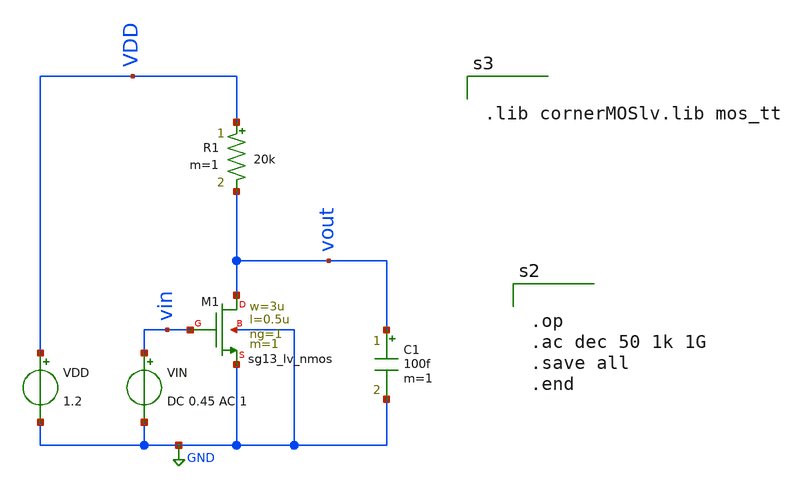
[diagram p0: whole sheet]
** sch_path: BTDay3-Ex/Ex1_Lecture3_1.sch
**.subckt Ex1_Lecture3_1
XM1 vout vin GND GND sg13_lv_nmos w=3u l=0.5u ng=1 m=1 mm_ok=1
VDD VDD GND 1.2
VIN vin GND DC 0.45 AC 1
R1 VDD vout 20k m=1
C1 vout GND 100f m=1
**** begin user architecture code


.op
.ac dec 50 1k 1G
.save all
.end




.lib cornerMOSlv.lib mos_tt


**** end user architecture code
**.ends
.GLOBAL GND
.end
